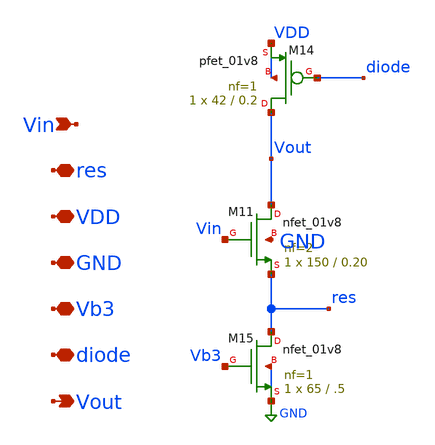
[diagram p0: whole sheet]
** sch_path: schem/cmfb_half.sch
**.subckt cmfb_half VDD GND Vout Vin diode Vb3 res
*.iopin VDD
*.iopin GND
*.opin Vout
*.ipin Vin
*.iopin diode
*.iopin Vb3
*.iopin res
XM11 Vout Vin res GND sky130_fd_pr__nfet_01v8 L=0.20 W=150 nf=2 ad='int((nf+1)/2) * W/nf * 0.29' as='int((nf+2)/2) * W/nf * 0.29'
+ pd='2*int((nf+1)/2) * (W/nf + 0.29)' ps='2*int((nf+2)/2) * (W/nf + 0.29)' nrd='0.29 / W' nrs='0.29 / W'
+ sa=0 sb=0 sd=0 mult=1 m=1
XM14 Vout diode VDD VDD sky130_fd_pr__pfet_01v8 L=0.2 W=42 nf=1 ad='int((nf+1)/2) * W/nf * 0.29' as='int((nf+2)/2) * W/nf * 0.29'
+ pd='2*int((nf+1)/2) * (W/nf + 0.29)' ps='2*int((nf+2)/2) * (W/nf + 0.29)' nrd='0.29 / W' nrs='0.29 / W'
+ sa=0 sb=0 sd=0 mult=1 m=1
XM15 res Vb3 GND GND sky130_fd_pr__nfet_01v8 L=.5 W=65 nf=1 ad='int((nf+1)/2) * W/nf * 0.29' as='int((nf+2)/2) * W/nf * 0.29'
+ pd='2*int((nf+1)/2) * (W/nf + 0.29)' ps='2*int((nf+2)/2) * (W/nf + 0.29)' nrd='0.29 / W' nrs='0.29 / W'
+ sa=0 sb=0 sd=0 mult=1 m=1
**.ends
.GLOBAL GND
.end
